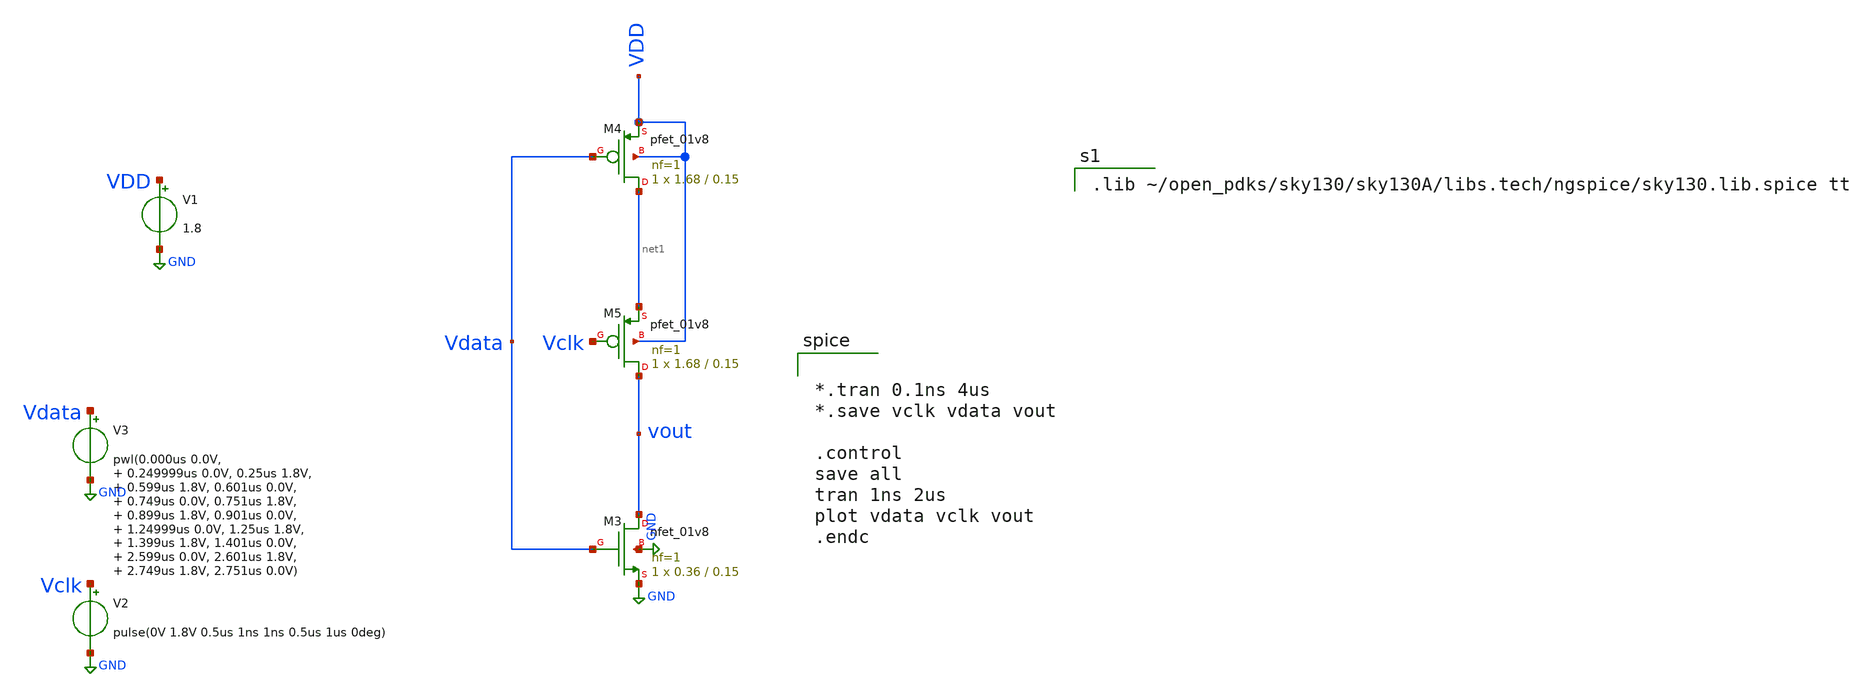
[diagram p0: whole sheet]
** sch_path: TSPC_Dff_firstStage.sch
**.subckt TSPC_Dff_firstStage
V1 VDD GND 1.8
V2 Vclk GND pulse(0V 1.8V 0.5us 1ns 1ns 0.5us 1us 0deg)
V3 Vdata GND pwl(0.000us 0.0V, 0.249999us 0.0V, 0.25us 1.8V, 0.599us 1.8V, 0.601us 0.0V, 0.749us
+ 0.0V, 0.751us 1.8V, 0.899us 1.8V, 0.901us 0.0V, 1.24999us 0.0V, 1.25us 1.8V, 1.399us 1.8V, 1.401us 0.0V,
+ 2.599us 0.0V, 2.601us 1.8V, 2.749us 1.8V, 2.751us 0.0V)
XM3 vout Vdata GND GND sky130_fd_pr__nfet_01v8 L=0.15 W=0.36 nf=1 ad='int((nf+1)/2) * W/nf * 0.29' as='int((nf+2)/2) * W/nf * 0.29'
+ pd='2*int((nf+1)/2) * (W/nf + 0.29)' ps='2*int((nf+2)/2) * (W/nf + 0.29)' nrd='0.29 / W' nrs='0.29 / W'
+ sa=0 sb=0 sd=0 mult=1 m=1
XM4 net1 Vdata VDD VDD sky130_fd_pr__pfet_01v8 L=0.15 W=1.68 nf=1 ad='int((nf+1)/2) * W/nf * 0.29' as='int((nf+2)/2) * W/nf * 0.29'
+ pd='2*int((nf+1)/2) * (W/nf + 0.29)' ps='2*int((nf+2)/2) * (W/nf + 0.29)' nrd='0.29 / W' nrs='0.29 / W'
+ sa=0 sb=0 sd=0 mult=1 m=1
XM5 vout Vclk net1 VDD sky130_fd_pr__pfet_01v8 L=0.15 W=1.68 nf=1 ad='int((nf+1)/2) * W/nf * 0.29' as='int((nf+2)/2) * W/nf * 0.29'
+ pd='2*int((nf+1)/2) * (W/nf + 0.29)' ps='2*int((nf+2)/2) * (W/nf + 0.29)' nrd='0.29 / W' nrs='0.29 / W'
+ sa=0 sb=0 sd=0 mult=1 m=1
**** begin user architecture code


*.tran 0.1ns 4us
*.save vclk vdata vout

.control
save all
tran 1ns 2us
plot vdata vclk vout
.endc



.lib ~/open_pdks/sky130/sky130A/libs.tech/ngspice/sky130.lib.spice tt

**** end user architecture code
**.ends
.GLOBAL GND
.end
